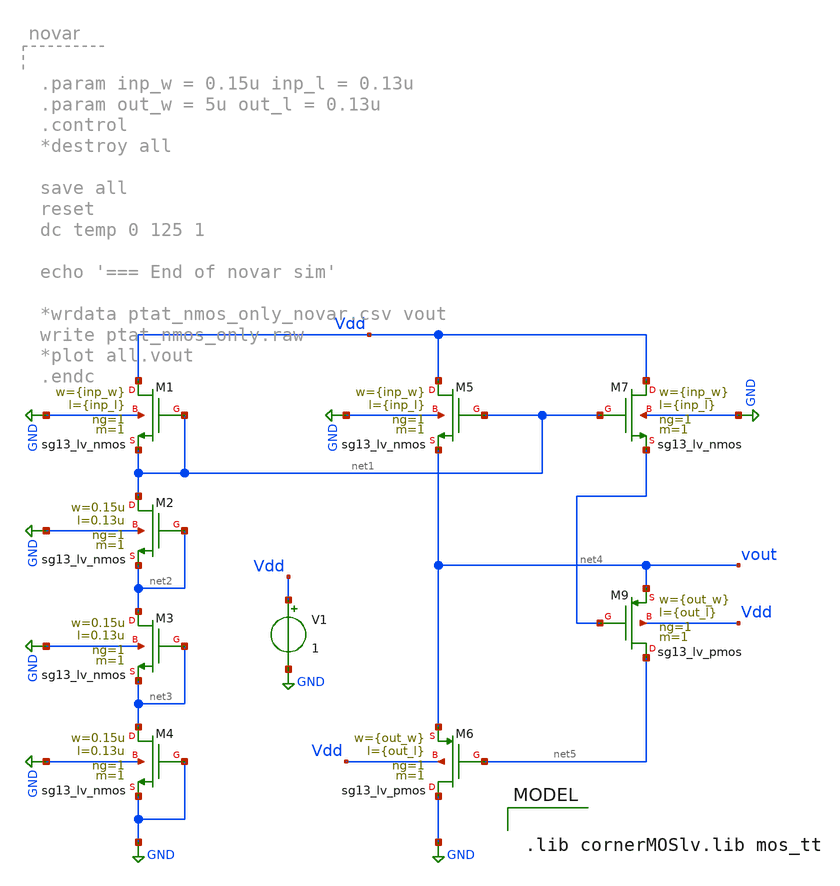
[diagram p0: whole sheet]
** sch_path: TempSensor/design_data/xschem/ptat_nmos_only.sch
**.subckt ptat_nmos_only
XM1 Vdd net1 net1 GND sg13_lv_nmos w={inp_w} l={inp_l} ng=1 m=1 mm_ok=1
XM2 net1 net2 net2 GND sg13_lv_nmos w=0.15u l=0.13u ng=1 m=1 mm_ok=1
XM3 net2 net3 net3 GND sg13_lv_nmos w=0.15u l=0.13u ng=1 m=1 mm_ok=1
XM4 net3 GND GND GND sg13_lv_nmos w=0.15u l=0.13u ng=1 m=1 mm_ok=1
XM5 Vdd net1 vout GND sg13_lv_nmos w={inp_w} l={inp_l} ng=1 m=1 mm_ok=1
XM7 Vdd net1 net4 GND sg13_lv_nmos w={inp_w} l={inp_l} ng=1 m=1 mm_ok=1
V1 Vdd GND 1
XM9 net5 net4 vout Vdd sg13_lv_pmos w={out_w} l={out_l} ng=1 m=1 mm_ok=1
XM6 GND net5 vout Vdd sg13_lv_pmos w={out_w} l={out_l} ng=1 m=1 mm_ok=1
**** begin user architecture code

.lib cornerMOSlv.lib mos_tt



.param inp_w = 0.15u inp_l = 0.13u
.param out_w = 0.15u out_l = 0.13u
.dc temp 0 125 1
.control

save all
reset

setplot new                  ; 'new' creates a new plot of some name
set myplot = $curplot        ; the new plot is stored in 'curplot'
let out = vector(2)

foreach varval 0.15u 0.3u 1u 2u
 alterparam inp_l = $varval
 echo '=== varval = $varval'
 reset
 run
 let {$myplot}.varinpl_out = vout

 write ptat_nmos_only.raw
 set appendwrite
end
unset appendwrite
.endc




.param inp_w = 0.15u inp_l = 0.13u
.param out_w = 0.15u out_l = 0.13u
.dc temp 0 125 1
.control

save all
reset

setplot new                  ; 'new' creates a new plot of some name
set myplot = $curplot        ; the new plot is stored in 'curplot'
let out = vector(2)

foreach varval 0.15u 0.3u 1u 2u
 alterparam inp_w = $varval
 echo '=== varval = $varval'
 reset
 run
 let {$myplot}.varinpw_out = vout

 write ptat_nmos_only.raw
 set appendwrite
end
unset appendwrite
.endc




.param inp_w = 0.15u inp_l = 0.13u
.param out_w = 0.15u out_l = 0.13u
.dc temp 0 125 1
.control

save all
reset

setplot new                  ; 'new' creates a new plot of some name
set myplot = $curplot        ; the new plot is stored in 'curplot'
let out = vector(2)

foreach varval 0.15u 0.3u 1u 2u
 alterparam out_w = $varval
 echo '=== varval = $varval'
 reset
 run
 let {$myplot}.varoutw_out = vout

 write ptat_nmos_only.raw
 set appendwrite
end
unset appendwrite
.endc




.param inp_w = 0.15u inp_l = 0.13u
.param out_w = 0.15u out_l = 0.13u
.dc temp 0 125 1
.control

save all
reset

setplot new                  ; 'new' creates a new plot of some name
set myplot = $curplot        ; the new plot is stored in 'curplot'
let out = vector(2)

foreach varval 0.15u 0.3u 1u 2u
 alterparam out_l = $varval
 echo '=== varval = $varval'
 reset
 run
 let {$myplot}.varoutl_out = vout

 write ptat_nmos_only.raw
 set appendwrite
end
unset appendwrite
.endc


**** end user architecture code
**.ends
.GLOBAL GND
.end
